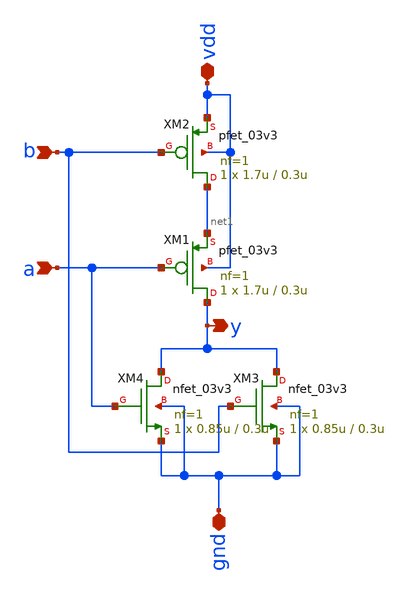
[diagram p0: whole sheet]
** sch_path: src/schematic/NOR/norGate.sch
**.subckt norGate gnd vdd a b y
*.iopin gnd
*.iopin vdd
*.ipin a
*.ipin b
*.opin y
XM1 y a net1 vdd pfet_03v3 L=0.3u W=1.7u nf=1 ad='int((nf+1)/2) * W/nf * 0.18u' as='int((nf+2)/2) * W/nf * 0.18u'
+ pd='2*int((nf+1)/2) * (W/nf + 0.18u)' ps='2*int((nf+2)/2) * (W/nf + 0.18u)' nrd='0.18u / W' nrs='0.18u / W'
+ sa=0 sb=0 sd=0 m=1
XM2 net1 b vdd vdd pfet_03v3 L=0.3u W=1.7u nf=1 ad='int((nf+1)/2) * W/nf * 0.18u' as='int((nf+2)/2) * W/nf * 0.18u'
+ pd='2*int((nf+1)/2) * (W/nf + 0.18u)' ps='2*int((nf+2)/2) * (W/nf + 0.18u)' nrd='0.18u / W' nrs='0.18u / W'
+ sa=0 sb=0 sd=0 m=1
XM3 y b gnd gnd nfet_03v3 L=0.3u W=0.85u nf=1 ad='int((nf+1)/2) * W/nf * 0.18u' as='int((nf+2)/2) * W/nf * 0.18u'
+ pd='2*int((nf+1)/2) * (W/nf + 0.18u)' ps='2*int((nf+2)/2) * (W/nf + 0.18u)' nrd='0.18u / W' nrs='0.18u / W'
+ sa=0 sb=0 sd=0 m=1
XM4 y a gnd gnd nfet_03v3 L=0.3u W=0.85u nf=1 ad='int((nf+1)/2) * W/nf * 0.18u' as='int((nf+2)/2) * W/nf * 0.18u'
+ pd='2*int((nf+1)/2) * (W/nf + 0.18u)' ps='2*int((nf+2)/2) * (W/nf + 0.18u)' nrd='0.18u / W' nrs='0.18u / W'
+ sa=0 sb=0 sd=0 m=1
**.ends
.end
